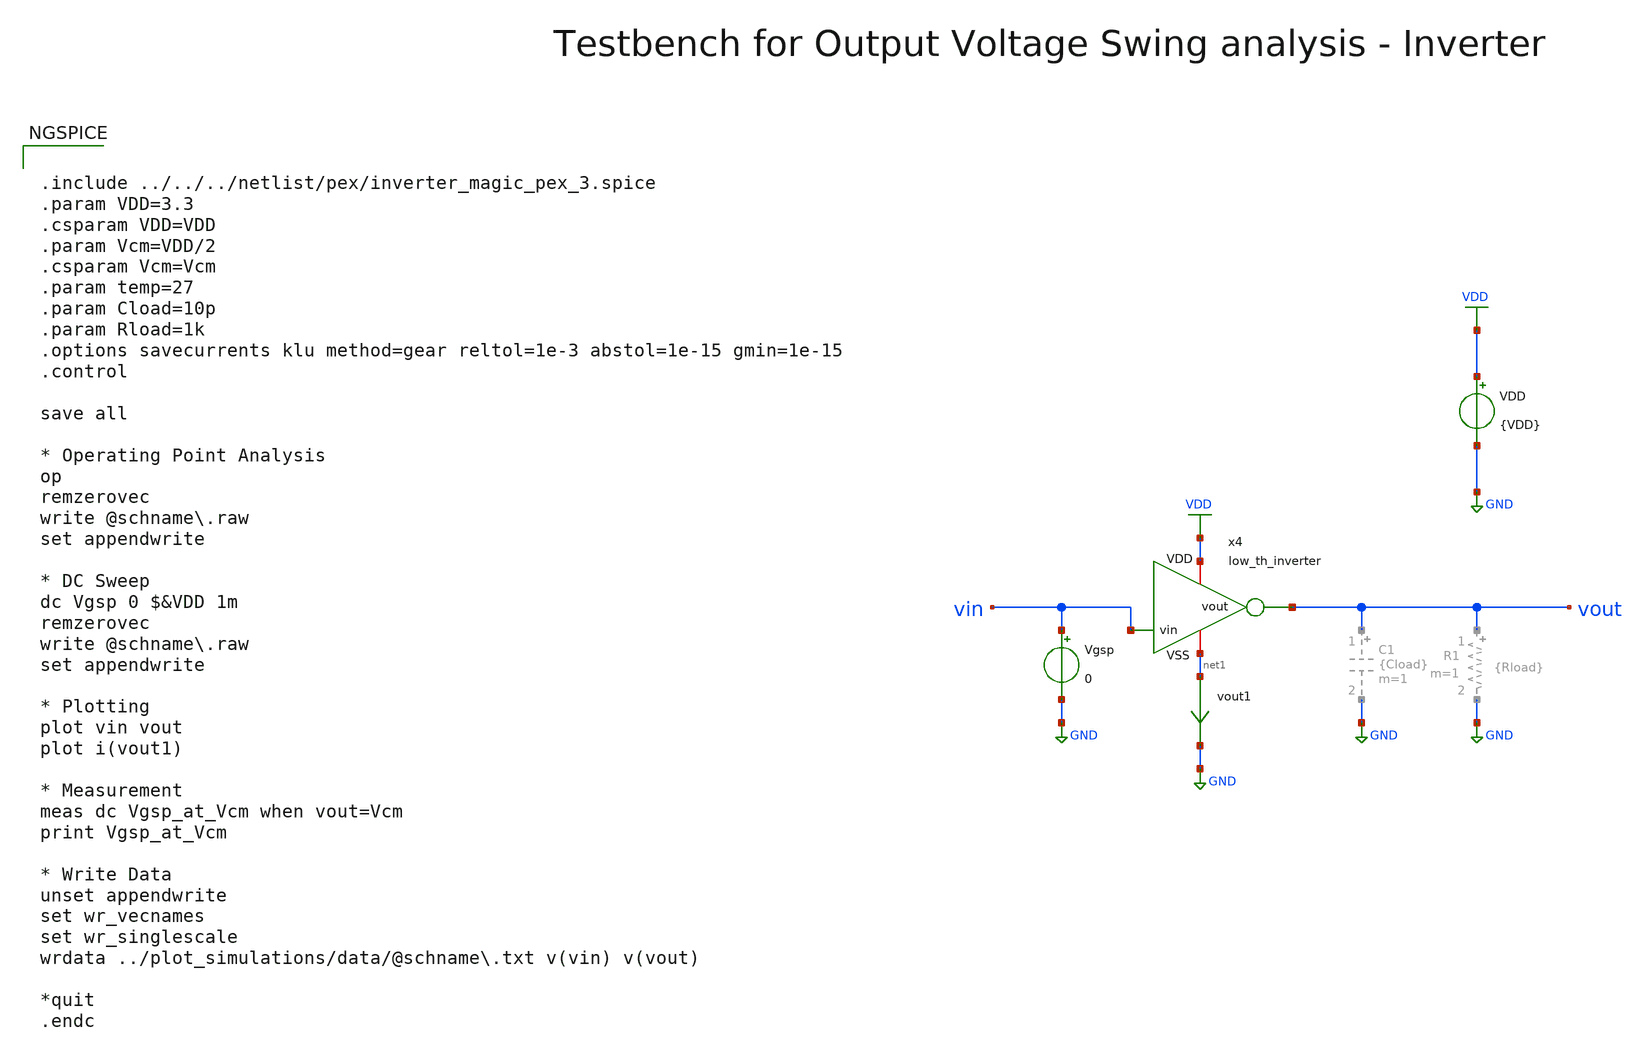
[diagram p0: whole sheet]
** sch_path: macros/heichips26_vcr/macros/switched_capacitor/testbenches/xschem/lth_inv_dc_vout.sch
**.subckt lth_inv_dc_vout
VDD VDD GND {VDD}
Vgsp vin GND 0
x4 VDD vin vout net1 low_th_inverter
vout1 net1 GND 0
.save i(vout1)
**** begin user architecture code


.include ../../../netlist/pex/inverter_magic_pex_3.spice
.param VDD=3.3
.csparam VDD=VDD
.param Vcm=VDD/2
.csparam Vcm=Vcm
.param temp=27
.param Cload=10p
.param Rload=1k
.options savecurrents klu method=gear reltol=1e-3 abstol=1e-15 gmin=1e-15
.control

save all

* Operating Point Analysis
op
remzerovec
write @schname\.raw
set appendwrite

* DC Sweep
dc Vgsp 0 $&VDD 1m
remzerovec
write @schname\.raw
set appendwrite

* Plotting
plot vin vout
plot i(vout1)

* Measurement
meas dc Vgsp_at_Vcm when vout=Vcm
print Vgsp_at_Vcm

* Write Data
unset appendwrite
set wr_vecnames
set wr_singlescale
wrdata ../plot_simulations/data/@schname\.txt v(vin) v(vout)

*quit
.endc



.lib cornerMOSlv.lib mos_tt
.lib cornerMOShv.lib mos_tt
.lib cornerRES.lib res_typ
.lib cornerDIO.lib dio_tt

**** end user architecture code
**.ends

* expanding   symbol:  low_th_inverter.sym # of pins=4
** sym_path: macros/heichips26_vcr/macros/switched_capacitor/schematic/xschem/low_th_inverter.sym
** sch_path: macros/heichips26_vcr/macros/switched_capacitor/schematic/xschem/low_th_inverter.sch
.subckt low_th_inverter VDD vin vout VSS
*.ipin vin
*.iopin VDD
*.iopin VSS
*.opin vout
XM1 vout vin VSS VSS sg13_hv_nmos w={n_ng*n_w} l={n_l} ng={n_ng} m=1 mm_ok=1
XM2 vout vin VDD VDD sg13_hv_pmos w={p_ng*p_w} l={p_l} ng={n_ng} m=1 mm_ok=1
**** begin user architecture code


.param n_ng = 2
.param n_w = 1u
.param n_l = 0.45u
.param p_ng = 2
.param p_w = 1u
.param p_l = 0.4u


**** end user architecture code
.ends

.GLOBAL GND
.GLOBAL VDD
.end
